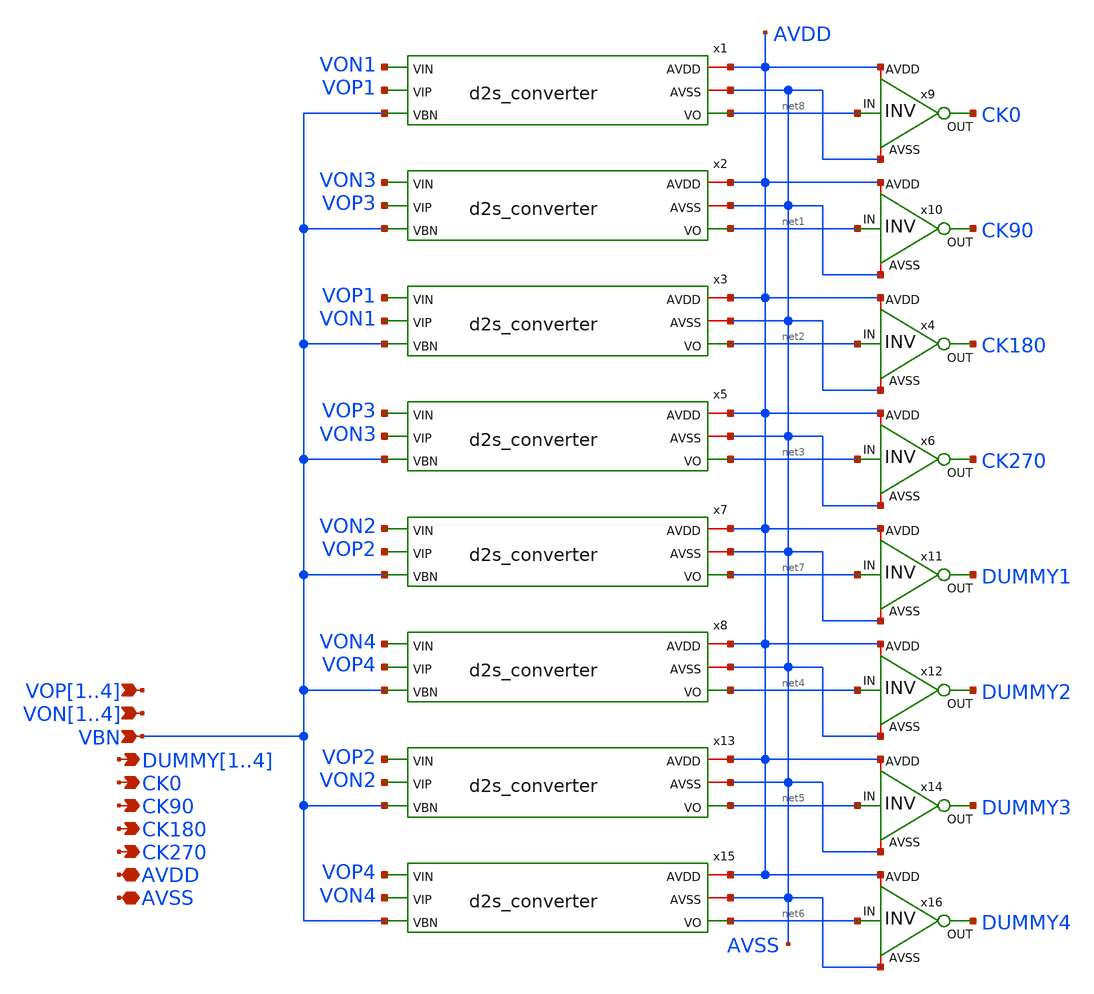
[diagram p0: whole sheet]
** sch_path: designs/libs/core_analog/d2s_top/d2s_top.sch
**.subckt d2s_top VOP1,VOP2,VOP3,VOP4 VON1,VON2,VON3,VON4 VBN DUMMY1,DUMMY2,DUMMY3,DUMMY4 CK0 CK90
*+ CK180 CK270 AVDD AVSS
*.ipin VOP1,VOP2,VOP3,VOP4
*.ipin VON1,VON2,VON3,VON4
*.ipin VBN
*.opin DUMMY1,DUMMY2,DUMMY3,DUMMY4
*.opin CK0
*.opin CK90
*.opin CK180
*.opin CK270
*.iopin AVDD
*.iopin AVSS
x1 AVDD AVSS VON1 VOP1 VBN net8 d2s_converter
x2 AVDD AVSS VON3 VOP3 VBN net1 d2s_converter
x9 AVDD net8 CK0 AVSS inv
x10 AVDD net1 CK90 AVSS inv
x3 AVDD AVSS VOP1 VON1 VBN net2 d2s_converter
x4 AVDD net2 CK180 AVSS inv
x5 AVDD AVSS VOP3 VON3 VBN net3 d2s_converter
x6 AVDD net3 CK270 AVSS inv
x7 AVDD AVSS VON2 VOP2 VBN net7 d2s_converter
x8 AVDD AVSS VON4 VOP4 VBN net4 d2s_converter
x11 AVDD net7 DUMMY1 AVSS inv
x12 AVDD net4 DUMMY2 AVSS inv
x13 AVDD AVSS VOP2 VON2 VBN net5 d2s_converter
x14 AVDD net5 DUMMY3 AVSS inv
x15 AVDD AVSS VOP4 VON4 VBN net6 d2s_converter
x16 AVDD net6 DUMMY4 AVSS inv
**.ends

* expanding   symbol:  libs/core_analog/d2s_converter/d2s_converter.sym # of pins=6
** sym_path: designs/libs/core_analog/d2s_converter/d2s_converter.sym
** sch_path: designs/libs/core_analog/d2s_converter/d2s_converter.sch
.subckt d2s_converter AVDD AVSS VIN VIP VBN VO
*.iopin AVDD
*.iopin AVSS
*.ipin VIN
*.ipin VIP
*.opin VO
*.ipin VBN
XM2 VOPB VIN i1 AVSS nfet_03v3 L=0.3u W=1.9u nf=1 ad='int((nf+1)/2) * W/nf * 0.18u' as='int((nf+2)/2) * W/nf * 0.18u'
+ pd='2*int((nf+1)/2) * (W/nf + 0.18u)' ps='2*int((nf+2)/2) * (W/nf + 0.18u)' nrd='0.18u / W' nrs='0.18u / W'
+ sa=0 sb=0 sd=0 m=4
XM4 VOPB VOPB AVDD AVDD pfet_03v3 L=0.3u W=1.4u nf=1 ad='int((nf+1)/2) * W/nf * 0.18u' as='int((nf+2)/2) * W/nf * 0.18u'
+ pd='2*int((nf+1)/2) * (W/nf + 0.18u)' ps='2*int((nf+2)/2) * (W/nf + 0.18u)' nrd='0.18u / W' nrs='0.18u / W'
+ sa=0 sb=0 sd=0 m=4
XM11 VOB VOB AVSS AVSS nfet_03v3 L=0.3u W=1.5u nf=1 ad='int((nf+1)/2) * W/nf * 0.18u' as='int((nf+2)/2) * W/nf * 0.18u'
+ pd='2*int((nf+1)/2) * (W/nf + 0.18u)' ps='2*int((nf+2)/2) * (W/nf + 0.18u)' nrd='0.18u / W' nrs='0.18u / W'
+ sa=0 sb=0 sd=0 m=4
XM13 VOB VOP AVDD AVDD pfet_03v3 L=0.3u W=2u nf=1 ad='int((nf+1)/2) * W/nf * 0.18u' as='int((nf+2)/2) * W/nf * 0.18u'
+ pd='2*int((nf+1)/2) * (W/nf + 0.18u)' ps='2*int((nf+2)/2) * (W/nf + 0.18u)' nrd='0.18u / W' nrs='0.18u / W'
+ sa=0 sb=0 sd=0 m=4
XM3 VOP VIP i1 AVSS nfet_03v3 L=0.3u W=1.9u nf=1 ad='int((nf+1)/2) * W/nf * 0.18u' as='int((nf+2)/2) * W/nf * 0.18u'
+ pd='2*int((nf+1)/2) * (W/nf + 0.18u)' ps='2*int((nf+2)/2) * (W/nf + 0.18u)' nrd='0.18u / W' nrs='0.18u / W'
+ sa=0 sb=0 sd=0 m=4
XM5 VOP VOPB AVDD AVDD pfet_03v3 L=0.3u W=1.4u nf=1 ad='int((nf+1)/2) * W/nf * 0.18u' as='int((nf+2)/2) * W/nf * 0.18u'
+ pd='2*int((nf+1)/2) * (W/nf + 0.18u)' ps='2*int((nf+2)/2) * (W/nf + 0.18u)' nrd='0.18u / W' nrs='0.18u / W'
+ sa=0 sb=0 sd=0 m=4
XM7 VONB VIP i2 AVSS nfet_03v3 L=0.3u W=1.9u nf=1 ad='int((nf+1)/2) * W/nf * 0.18u' as='int((nf+2)/2) * W/nf * 0.18u'
+ pd='2*int((nf+1)/2) * (W/nf + 0.18u)' ps='2*int((nf+2)/2) * (W/nf + 0.18u)' nrd='0.18u / W' nrs='0.18u / W'
+ sa=0 sb=0 sd=0 m=4
XM8 VONB VONB AVDD AVDD pfet_03v3 L=0.3u W=1.4u nf=1 ad='int((nf+1)/2) * W/nf * 0.18u' as='int((nf+2)/2) * W/nf * 0.18u'
+ pd='2*int((nf+1)/2) * (W/nf + 0.18u)' ps='2*int((nf+2)/2) * (W/nf + 0.18u)' nrd='0.18u / W' nrs='0.18u / W'
+ sa=0 sb=0 sd=0 m=4
XM9 VON VIN i2 AVSS nfet_03v3 L=0.3u W=1.9u nf=1 ad='int((nf+1)/2) * W/nf * 0.18u' as='int((nf+2)/2) * W/nf * 0.18u'
+ pd='2*int((nf+1)/2) * (W/nf + 0.18u)' ps='2*int((nf+2)/2) * (W/nf + 0.18u)' nrd='0.18u / W' nrs='0.18u / W'
+ sa=0 sb=0 sd=0 m=4
XM10 VON VONB AVDD AVDD pfet_03v3 L=0.3u W=1.4u nf=1 ad='int((nf+1)/2) * W/nf * 0.18u' as='int((nf+2)/2) * W/nf * 0.18u'
+ pd='2*int((nf+1)/2) * (W/nf + 0.18u)' ps='2*int((nf+2)/2) * (W/nf + 0.18u)' nrd='0.18u / W' nrs='0.18u / W'
+ sa=0 sb=0 sd=0 m=4
XM14 VO VON AVDD AVDD pfet_03v3 L=0.3u W=2u nf=1 ad='int((nf+1)/2) * W/nf * 0.18u' as='int((nf+2)/2) * W/nf * 0.18u'
+ pd='2*int((nf+1)/2) * (W/nf + 0.18u)' ps='2*int((nf+2)/2) * (W/nf + 0.18u)' nrd='0.18u / W' nrs='0.18u / W'
+ sa=0 sb=0 sd=0 m=4
XM12 VO VOB AVSS AVSS nfet_03v3 L=0.3u W=1.5u nf=1 ad='int((nf+1)/2) * W/nf * 0.18u' as='int((nf+2)/2) * W/nf * 0.18u'
+ pd='2*int((nf+1)/2) * (W/nf + 0.18u)' ps='2*int((nf+2)/2) * (W/nf + 0.18u)' nrd='0.18u / W' nrs='0.18u / W'
+ sa=0 sb=0 sd=0 m=4
XM1 i1 VBN AVSS AVSS nfet_03v3 L=0.5u W=11.25u nf=1 ad='int((nf+1)/2) * W/nf * 0.18u' as='int((nf+2)/2) * W/nf * 0.18u'
+ pd='2*int((nf+1)/2) * (W/nf + 0.18u)' ps='2*int((nf+2)/2) * (W/nf + 0.18u)' nrd='0.18u / W' nrs='0.18u / W'
+ sa=0 sb=0 sd=0 m=4
XM6 i2 VBN AVSS AVSS nfet_03v3 L=0.5u W=11.25u nf=1 ad='int((nf+1)/2) * W/nf * 0.18u' as='int((nf+2)/2) * W/nf * 0.18u'
+ pd='2*int((nf+1)/2) * (W/nf + 0.18u)' ps='2*int((nf+2)/2) * (W/nf + 0.18u)' nrd='0.18u / W' nrs='0.18u / W'
+ sa=0 sb=0 sd=0 m=4
.ends


* expanding   symbol:  libs/core_analog/inv/inv.sym # of pins=4
** sym_path: designs/libs/core_analog/inv/inv.sym
** sch_path: designs/libs/core_analog/inv/inv.sch
.subckt inv AVDD IN OUT AVSS
*.ipin IN
*.iopin AVDD
*.iopin AVSS
*.opin OUT
XM1 OUT IN AVDD AVDD pfet_03v3 L=0.28u W=0.9u nf=1 ad='int((nf+1)/2) * W/nf * 0.18u' as='int((nf+2)/2) * W/nf * 0.18u'
+ pd='2*int((nf+1)/2) * (W/nf + 0.18u)' ps='2*int((nf+2)/2) * (W/nf + 0.18u)' nrd='0.18u / W' nrs='0.18u / W'
+ sa=0 sb=0 sd=0 m=1
XM2 OUT IN AVSS AVSS nfet_03v3 L=0.28u W=0.3u nf=1 ad='int((nf+1)/2) * W/nf * 0.18u' as='int((nf+2)/2) * W/nf * 0.18u'
+ pd='2*int((nf+1)/2) * (W/nf + 0.18u)' ps='2*int((nf+2)/2) * (W/nf + 0.18u)' nrd='0.18u / W' nrs='0.18u / W'
+ sa=0 sb=0 sd=0 m=1
.ends

.end
